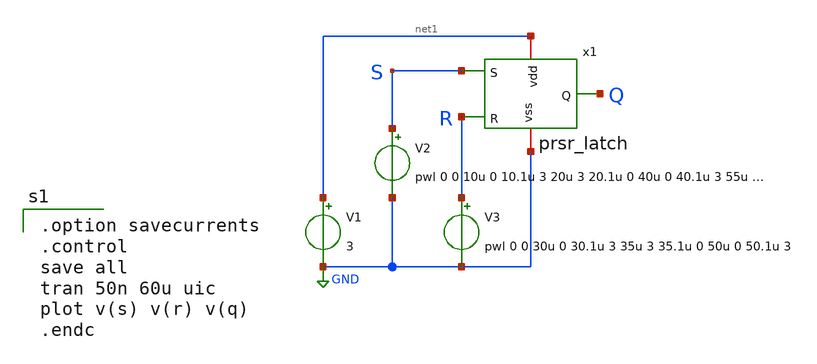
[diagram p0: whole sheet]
** sch_path: member_project/DCDC/ShuntaroOHNO/xschem/prsr_latch_tran.sch
**.subckt prsr_latch_tran
x1 net1 Q S R GND prsr_latch
V1 net1 GND 3
V2 S GND pwl 0 0 10u 0 10.1u 3 20u 3 20.1u 0 40u 0 40.1u 3 55u 3 55.1u 0
V3 R GND pwl 0 0 30u 0 30.1u 3 35u 3 35.1u 0 50u 0 50.1u 3
**** begin user architecture code
 .include $::LIB/ip62_models

.option savecurrents
.control
save all
tran 50n 60u uic
plot v(s) v(r) v(q)
.endc

**** end user architecture code
**.ends

* expanding   symbol:  prsr_latch.sym # of pins=5
** sym_path: member_project/Tiny555/yamada3/xschem/prsr_latch.sym
** sch_path: member_project/Tiny555/yamada3/xschem/prsr_latch.sch
.subckt prsr_latch vdd Q S R vss
*.iopin vdd
*.iopin vss
*.ipin S
*.ipin R
*.opin Q
XXM1 net2 R vdd vdd PMOS w=10u l=1u as=0 ad=0 ps=0 pd=0 nrd=0 nrs=0 m=1
XXM2 Q net1 net2 vdd PMOS w=10u l=1u as=0 ad=0 ps=0 pd=0 nrd=0 nrs=0 m=1
XXM3 Q R vss vss NMOS w=3.4u l=1u as=0 ad=0 ps=0 pd=0 nrd=0 nrs=0 m=1
XXM4 Q net1 vss vss NMOS w=3.4u l=1u as=0 ad=0 ps=0 pd=0 nrd=0 nrs=0 m=1
XXM5 net3 R vdd vdd PMOS w=10u l=1u as=0 ad=0 ps=0 pd=0 nrd=0 nrs=0 m=1
XXM6 net3 R vss vss NMOS w=3.4u l=1u as=0 ad=0 ps=0 pd=0 nrd=0 nrs=0 m=1
XXM7 net5 Q vdd vdd PMOS w=10u l=1u as=0 ad=0 ps=0 pd=0 nrd=0 nrs=0 m=1
XXM8 net1 S net5 vdd PMOS w=10u l=1u as=0 ad=0 ps=0 pd=0 nrd=0 nrs=0 m=1
XXM9 net1 net3 net5 vdd PMOS w=10u l=1u as=0 ad=0 ps=0 pd=0 nrd=0 nrs=0 m=1
XXM10 net1 S net4 vss NMOS w=3.4u l=1u as=0 ad=0 ps=0 pd=0 nrd=0 nrs=0 m=1
XXM11 net1 Q vss vss NMOS w=3.4u l=1u as=0 ad=0 ps=0 pd=0 nrd=0 nrs=0 m=1
XXM12 net4 net3 vss vss NMOS w=3.4u l=1u as=0 ad=0 ps=0 pd=0 nrd=0 nrs=0 m=1
.ends

.GLOBAL GND
.end
